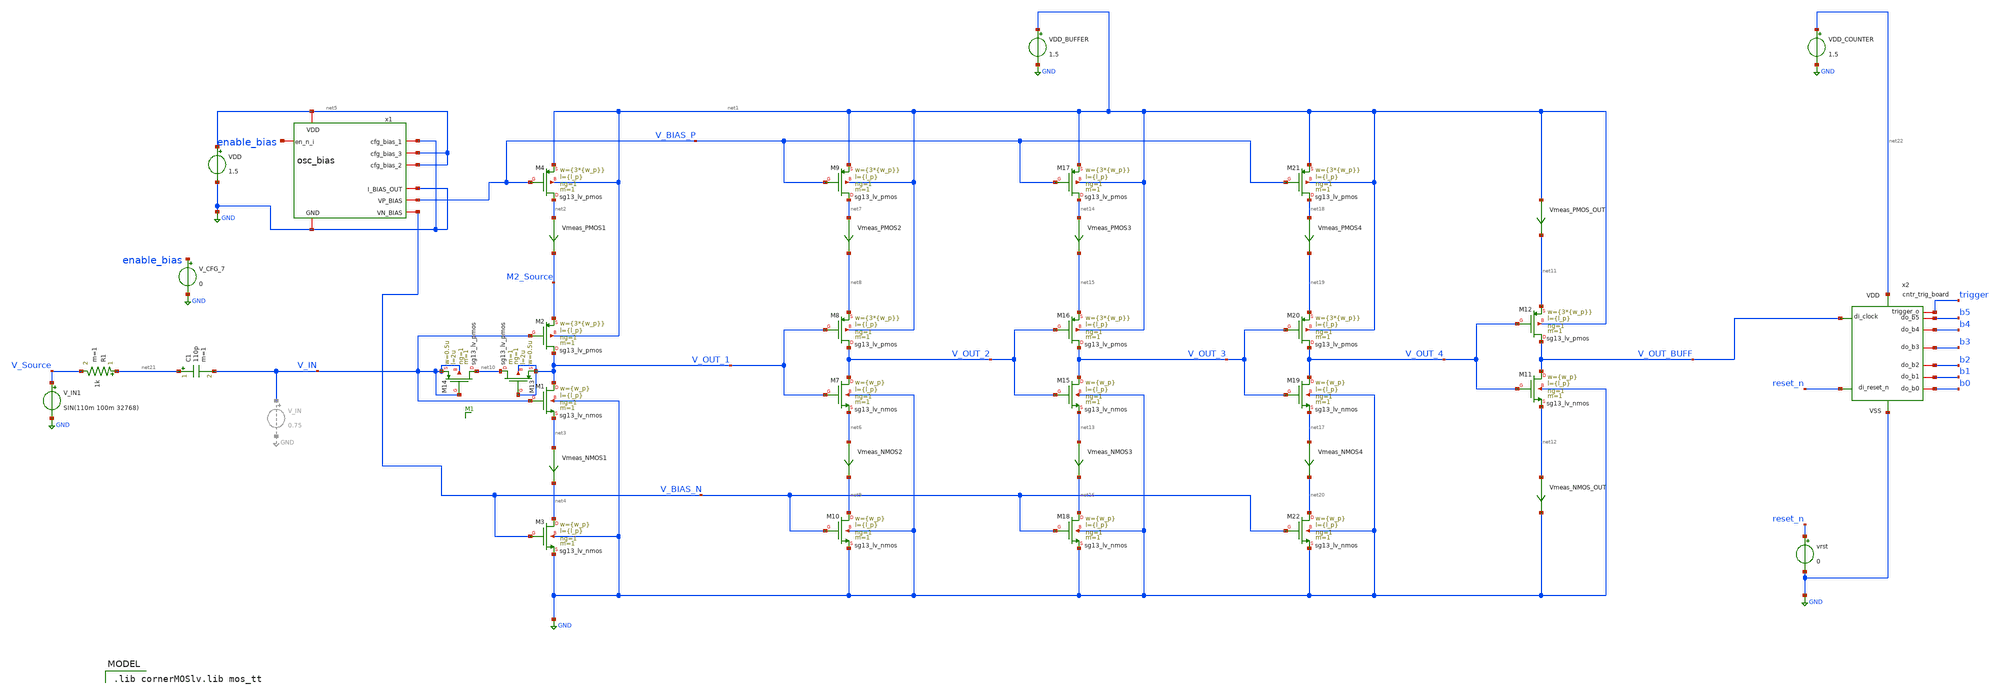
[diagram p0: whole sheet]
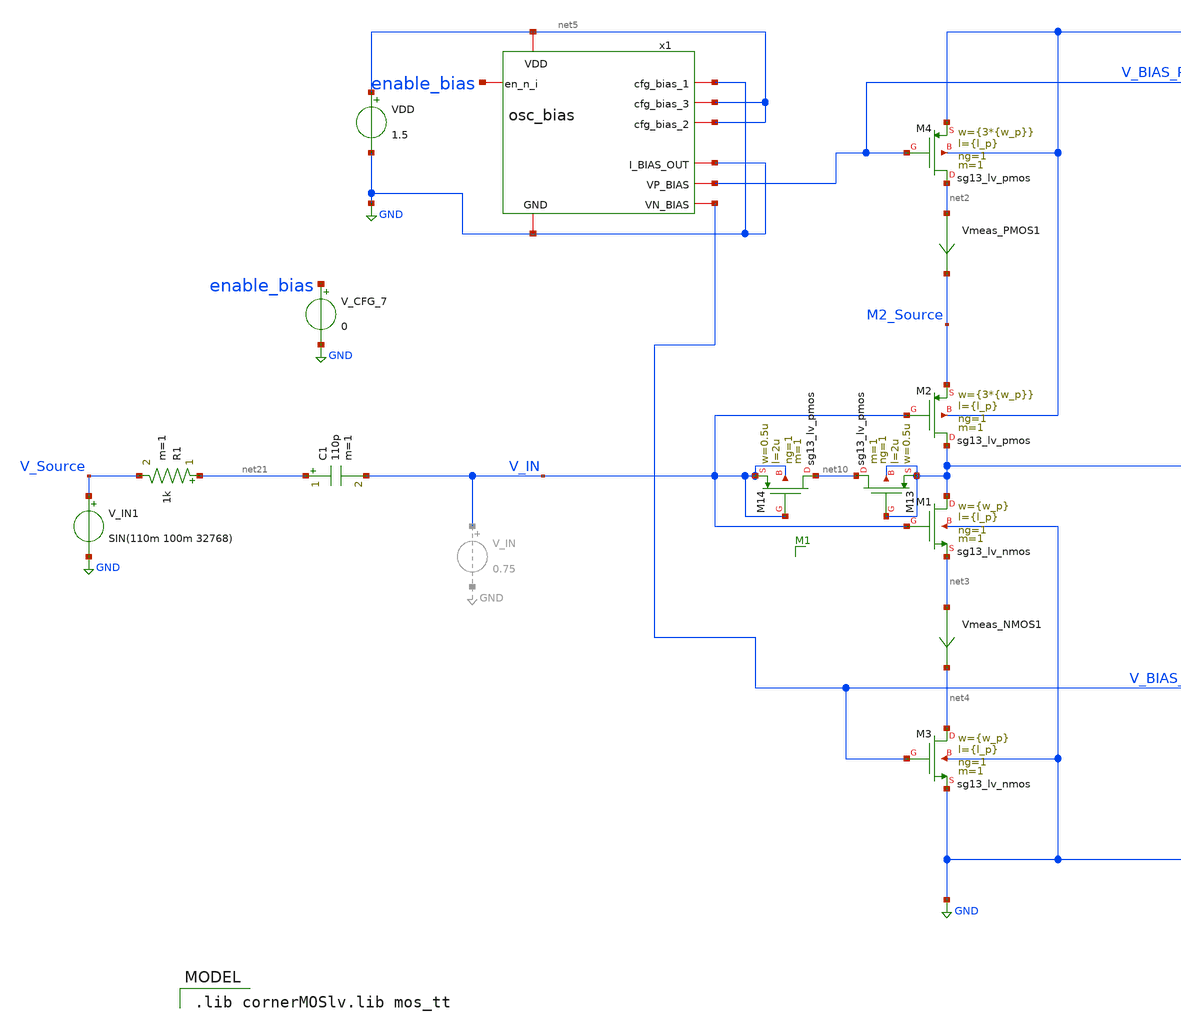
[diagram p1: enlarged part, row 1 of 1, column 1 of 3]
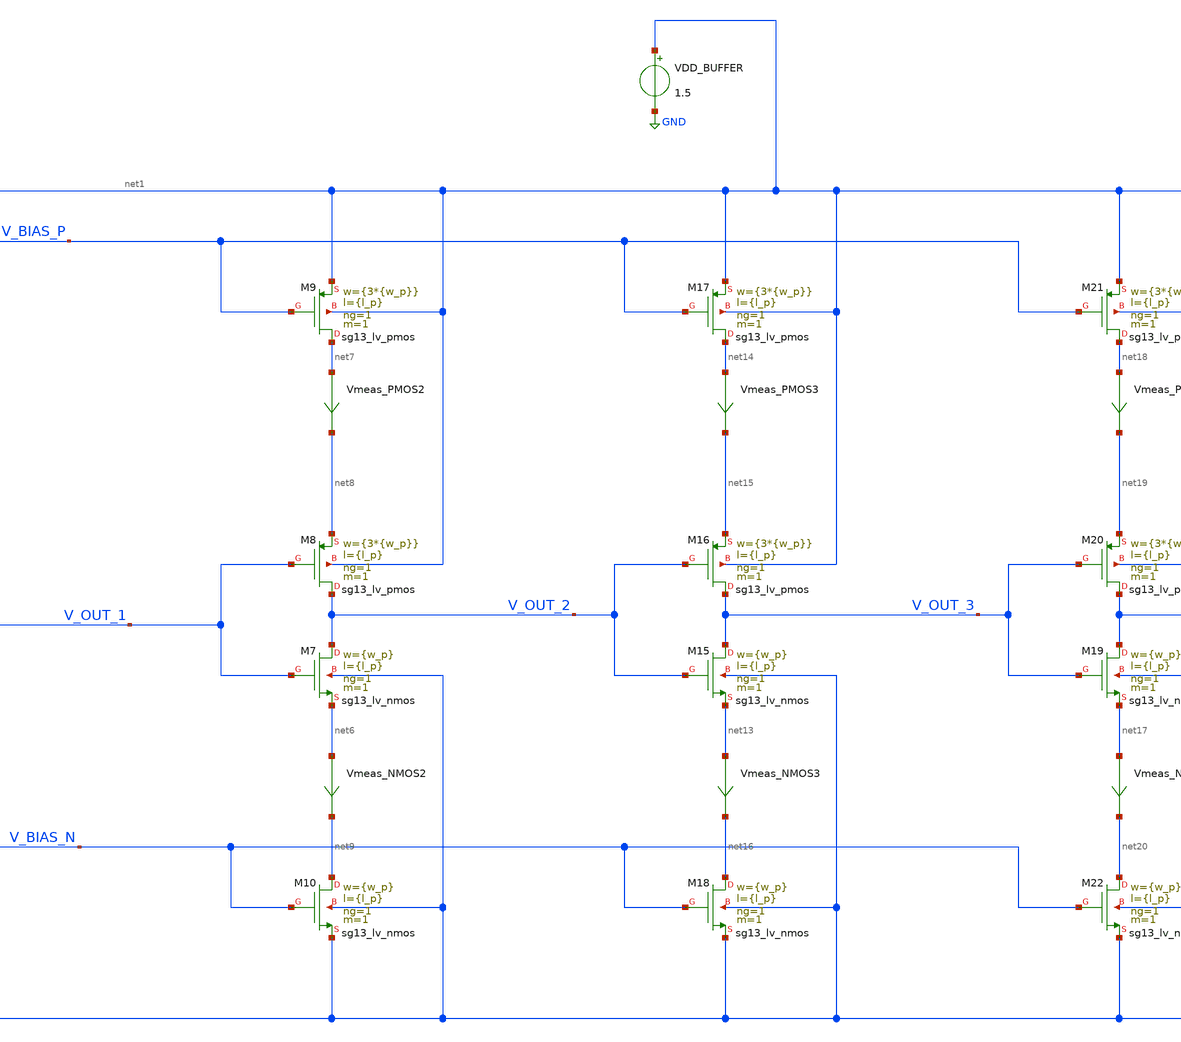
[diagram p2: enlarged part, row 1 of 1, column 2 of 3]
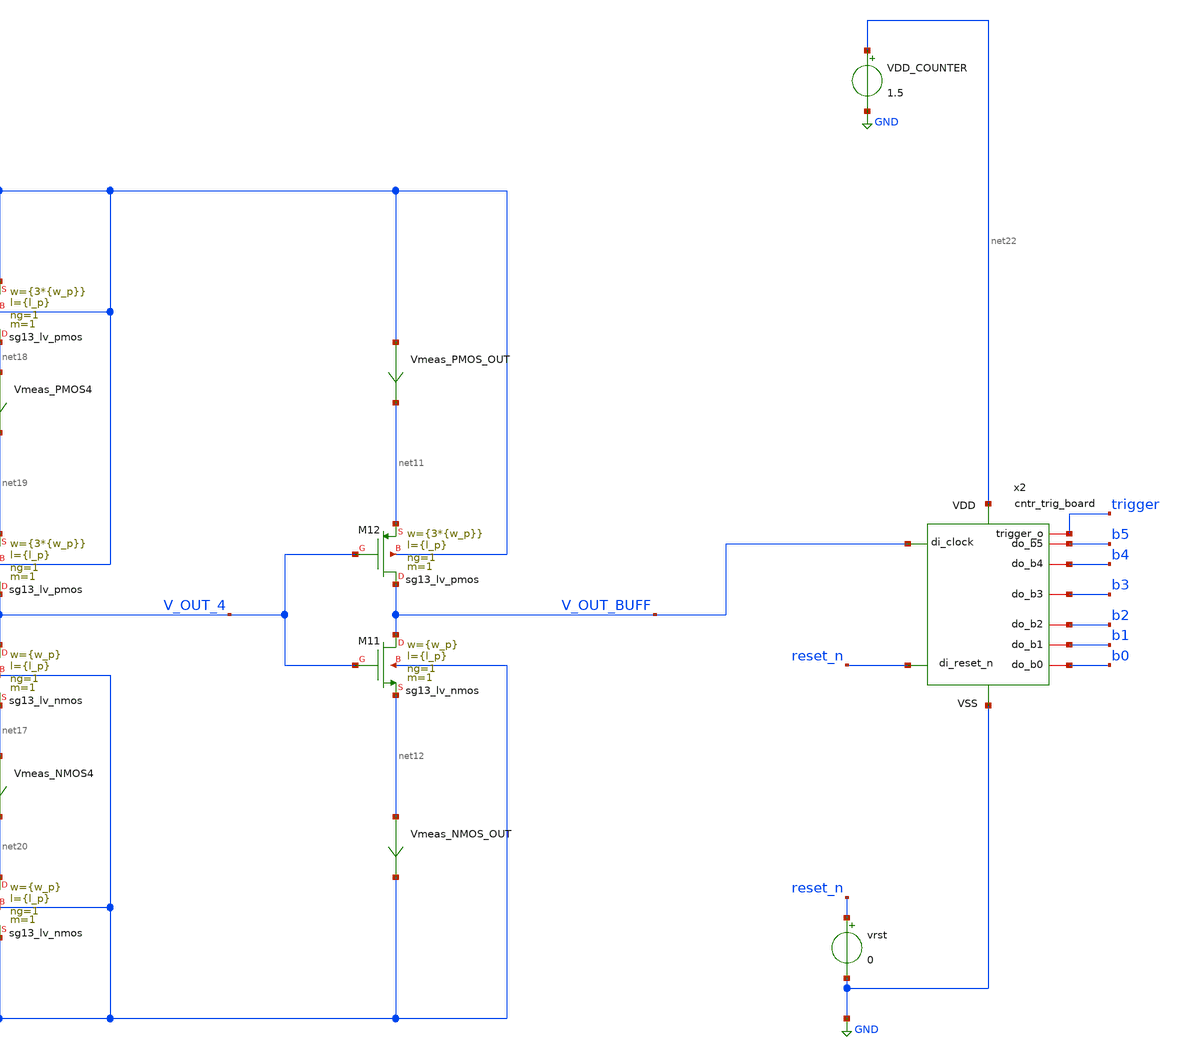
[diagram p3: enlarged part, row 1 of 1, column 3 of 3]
** sch_path: inverter_starved_v2_playground.sch
**.subckt inverter_starved_v2_playground
XM1 V_OUT_1 V_IN net3 GND sg13_lv_nmos w={w_p} l={l_p} ng=1 m=1 mm_ok=1
XM2 V_OUT_1 V_IN M2_Source net1 sg13_lv_pmos w={3*{w_p}} l={l_p} ng=1 m=1 mm_ok=1
VDD net5 GND 1.5
XM3 net4 V_BIAS_N GND GND sg13_lv_nmos w={w_p} l={l_p} ng=1 m=1 mm_ok=1
XM4 net2 V_BIAS_P net1 net1 sg13_lv_pmos w={3*{w_p}} l={l_p} ng=1 m=1 mm_ok=1
Vmeas_PMOS1 net2 M2_Source 0
.save i(vmeas_pmos1)
Vmeas_NMOS1 net3 net4 0
.save i(vmeas_nmos1)
V_IN1 V_Source GND SIN(110m 100m 32768)
C1 net21 V_IN 110p m=1
XM7 V_OUT_2 V_OUT_1 net6 GND sg13_lv_nmos w={w_p} l={l_p} ng=1 m=1 mm_ok=1
XM8 V_OUT_2 V_OUT_1 net8 net1 sg13_lv_pmos w={3*{w_p}} l={l_p} ng=1 m=1 mm_ok=1
Vmeas_NMOS2 net6 net9 0
.save i(vmeas_nmos2)
XM9 net7 V_BIAS_P net1 net1 sg13_lv_pmos w={3*{w_p}} l={l_p} ng=1 m=1 mm_ok=1
Vmeas_PMOS2 net7 net8 0
.save i(vmeas_pmos2)
XM10 net9 V_BIAS_N GND GND sg13_lv_nmos w={w_p} l={l_p} ng=1 m=1 mm_ok=1
XM11 V_OUT_BUFF V_OUT_4 net12 GND sg13_lv_nmos w={w_p} l={l_p} ng=1 m=1 mm_ok=1
XM12 V_OUT_BUFF V_OUT_4 net11 net1 sg13_lv_pmos w={3*{w_p}} l={l_p} ng=1 m=1 mm_ok=1
XM13 net10 V_OUT_1 V_OUT_1 V_OUT_1 sg13_lv_pmos w=0.5u l=2u ng=1 m=1 mm_ok=1
XM14 net10 V_IN V_IN V_IN sg13_lv_pmos w=0.5u l=2u ng=1 m=1 mm_ok=1
Vmeas_PMOS_OUT net1 net11 0
.save i(vmeas_pmos_out)
Vmeas_NMOS_OUT net12 GND 0
.save i(vmeas_nmos_out)
XM15 V_OUT_3 V_OUT_2 net13 GND sg13_lv_nmos w={w_p} l={l_p} ng=1 m=1 mm_ok=1
XM16 V_OUT_3 V_OUT_2 net15 net1 sg13_lv_pmos w={3*{w_p}} l={l_p} ng=1 m=1 mm_ok=1
Vmeas_NMOS3 net13 net16 0
.save i(vmeas_nmos3)
XM17 net14 V_BIAS_P net1 net1 sg13_lv_pmos w={3*{w_p}} l={l_p} ng=1 m=1 mm_ok=1
Vmeas_PMOS3 net14 net15 0
.save i(vmeas_pmos3)
XM18 net16 V_BIAS_N GND GND sg13_lv_nmos w={w_p} l={l_p} ng=1 m=1 mm_ok=1
XM19 V_OUT_4 V_OUT_3 net17 GND sg13_lv_nmos w={w_p} l={l_p} ng=1 m=1 mm_ok=1
XM20 V_OUT_4 V_OUT_3 net19 net1 sg13_lv_pmos w={3*{w_p}} l={l_p} ng=1 m=1 mm_ok=1
Vmeas_NMOS4 net17 net20 0
.save i(vmeas_nmos4)
XM21 net18 V_BIAS_P net1 net1 sg13_lv_pmos w={3*{w_p}} l={l_p} ng=1 m=1 mm_ok=1
Vmeas_PMOS4 net18 net19 0
.save i(vmeas_pmos4)
XM22 net20 V_BIAS_N GND GND sg13_lv_nmos w={w_p} l={l_p} ng=1 m=1 mm_ok=1
x1 net5 GND net5 net5 GND GND V_BIAS_P V_BIAS_N enable_bias osc_bias
x2 net22 GND V_OUT_BUFF b0 b1 b2 b3 b4 b5 reset_n trigger cntr_trig_board
vrst reset_n GND 0
V_CFG_7 enable_bias GND 0
R1 net21 V_Source 1k m=1
VDD_BUFFER net1 GND 1.5
VDD_COUNTER net22 GND 1.5
**** begin user architecture code
 .lib cornerMOSlv.lib mos_tt



.include inverter_starved_v2_playground.save
.include /foss/designs/xtal/xspice/cntr_trig_board.xspice
.param w_p=0.35u l_p=0.14u
.meas tran iavg_stage_1_pmos AVG i(Vmeas_PMOS1)
.meas tran iavg_stage_1_nmos AVG i(Vmeas_NMOS2)
.meas tran iavg_stage_2_pmos AVG i(Vmeas_PMOS2)
.meas tran iavg_stage_2_nmos AVG i(Vmeas_NMOS2)
.meas tran iavg_stage_3_pmos AVG i(Vmeas_PMOS3)
.meas tran iavg_stage_3_nmos AVG i(Vmeas_NMOS3)
.meas tran iavg_stage_4_pmos AVG i(Vmeas_PMOS4)
.meas tran iavg_stage_4_nmos AVG i(Vmeas_NMOS4)
.meas tran iavg_stage_5_pmos AVG i(Vmeas_PMOS_OUT)
.meas tran iavg_stage_5_nmos AVG i(Vmeas_NMOS_OUT)
.meas tran iavg_VDD AVG i(VDD)
.meas tran iavg_VDD_BUFFER AVG i(VDD_BUFFER)
.meas tran iavg_VDD_COUNTER AVG i(VDD_COUNTER)

.control
save all


tran 0.1u 0.3m
write inverter_starved_v2_playground.raw

plot V_Source V_IN V_OUT_1 V_OUT_2 V_OUT_3 V_OUT_4 V_OUT_BUFF
*plot V_IN V_OUT_BUFF


*fft V_OUT_3
*plot mag(V_OUT_3)

*.measure tran yrms RMS i(VDD) from=0.1m to=0.2m

set wr_singlescale
set wr_vecnames

wrdata clock_buffer.txt V_Source V_IN V_OUT_1 V_OUT_2 V_OUT_3 V_OUT_4 V_OUT_BUFF

.endc


**** end user architecture code
**.ends

* expanding   symbol:  osc_bias.sym # of pins=9
** sym_path: osc_bias.sym
** sch_path: osc_bias.sch
.subckt osc_bias VDD cfg_bias_1 cfg_bias_3 cfg_bias_2 GND I_BIAS_OUT VP_BIAS VN_BIAS en_n_i
*.iopin VDD
*.iopin GND
*.iopin I_BIAS_OUT
*.iopin cfg_bias_1
*.iopin cfg_bias_2
*.iopin cfg_bias_3
*.opin VN_BIAS
*.opin VP_BIAS
*.iopin en_n_i
XM1 net1 net1 VS_M1 VDD sg13_lv_pmos w=0.25u l=10u ng=1 m=1 mm_ok=1
XM3 net1 net1 net2 GND sg13_lv_nmos w=0.25u l=10u ng=1 m=1 mm_ok=1
XM4 net2 net2 net3 GND sg13_lv_nmos w=0.25u l=10u ng=1 m=1 mm_ok=1
XM5 net3 net3 net14 GND sg13_lv_nmos w=0.25u l=10u ng=1 m=1 mm_ok=1
XM2 net9 net1 VS_M2 VDD sg13_lv_pmos w=0.25u l=10u ng=1 m=2 mm_ok=1
XM6 net4 cfg_bias_1 net9 VDD sg13_lv_pmos w=0.25u l=10u ng=1 m=1 mm_ok=1
XM7 net5 net1 net15 VDD sg13_lv_pmos w=0.25u l=10u ng=1 m=4 mm_ok=1
XM8 net6 net1 net16 VDD sg13_lv_pmos w=0.25u l=10u ng=1 m=8 mm_ok=1
XM9 net4 cfg_bias_2 net5 VDD sg13_lv_pmos w=0.25u l=10u ng=1 m=1 mm_ok=1
XM10 net4 cfg_bias_3 net6 VDD sg13_lv_pmos w=0.25u l=10u ng=1 m=1 mm_ok=1
XM11 net7 net7 net8 GND sg13_lv_nmos w=0.25u l=10u ng=1 m=1 mm_ok=1
Vmeas net8 GND 0
.save i(vmeas)
XM12 VP_BIAS VP_BIAS net12 VDD sg13_lv_pmos w=1.05u l=0.14u ng=1 m=1 mm_ok=1
XM13 VN_BIAS VN_BIAS net11 GND sg13_lv_nmos w=0.35u l=0.14u ng=1 m=1 mm_ok=1
Vmeas1 VS_M12 net12 0
.save i(vmeas1)
Vmeas2 net11 GND 0
.save i(vmeas2)
XM14 net10 net10 VN_BIAS GND sg13_lv_nmos w=0.35u l=8u ng=1 m=1 mm_ok=1
XM15 net13 net13 net10 GND sg13_lv_nmos w=0.35u l=8u ng=1 m=1 mm_ok=1
XM16 VP_BIAS VP_BIAS net13 GND sg13_lv_nmos w=0.35u l=8u ng=1 m=1 mm_ok=1
XM17 net14 net14 net7 GND sg13_lv_nmos w=0.25u l=10u ng=1 m=1 mm_ok=1
Vmeas3 net4 I_BIAS_OUT 0
.save i(vmeas3)
XM18 VS_M1 en_n_i VDD VDD sg13_lv_pmos w=1u l=0.13u ng=1 m=1 mm_ok=1
XM19 VS_M2 en_n_i VDD VDD sg13_lv_pmos w=1u l=0.13u ng=1 m=1 mm_ok=1
XM20 net15 en_n_i VDD VDD sg13_lv_pmos w=1u l=0.13u ng=1 m=1 mm_ok=1
XM21 net16 en_n_i VDD VDD sg13_lv_pmos w=1u l=0.13u ng=1 m=1 mm_ok=1
XM22 VS_M12 en_n_i VDD VDD sg13_lv_pmos w=1u l=0.13u ng=1 m=1 mm_ok=1
.ends

.GLOBAL GND
.end
